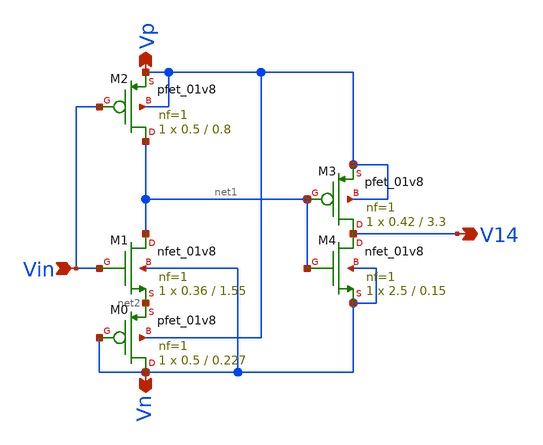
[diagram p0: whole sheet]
** sch_path: xschem/Vth_sch/Symbol/th14.sch
**.subckt th14 Vn Vp Vin V14
*.opin Vn
*.opin Vp
*.ipin Vin
*.opin V14
XM3 V14 net1 Vp Vp sky130_fd_pr__pfet_01v8 L=3.3 W=0.42 nf=1 ad='int((nf+1)/2) * W/nf * 0.29' as='int((nf+2)/2) * W/nf * 0.29'
+ pd='2*int((nf+1)/2) * (W/nf + 0.29)' ps='2*int((nf+2)/2) * (W/nf + 0.29)' nrd='0.29 / W' nrs='0.29 / W'
+ sa=0 sb=0 sd=0 mult=1 m=1
XM4 V14 net1 Vn Vn sky130_fd_pr__nfet_01v8 L=0.15 W=2.5 nf=1 ad='int((nf+1)/2) * W/nf * 0.29' as='int((nf+2)/2) * W/nf * 0.29'
+ pd='2*int((nf+1)/2) * (W/nf + 0.29)' ps='2*int((nf+2)/2) * (W/nf + 0.29)' nrd='0.29 / W' nrs='0.29 / W'
+ sa=0 sb=0 sd=0 mult=1 m=1
XM2 net1 Vin Vp Vp sky130_fd_pr__pfet_01v8 L=0.8 W=0.5 nf=1 ad='int((nf+1)/2) * W/nf * 0.29' as='int((nf+2)/2) * W/nf * 0.29'
+ pd='2*int((nf+1)/2) * (W/nf + 0.29)' ps='2*int((nf+2)/2) * (W/nf + 0.29)' nrd='0.29 / W' nrs='0.29 / W'
+ sa=0 sb=0 sd=0 mult=1 m=1
XM1 net1 Vin net2 Vn sky130_fd_pr__nfet_01v8 L=1.55 W=0.36 nf=1 ad='int((nf+1)/2) * W/nf * 0.29' as='int((nf+2)/2) * W/nf * 0.29'
+ pd='2*int((nf+1)/2) * (W/nf + 0.29)' ps='2*int((nf+2)/2) * (W/nf + 0.29)' nrd='0.29 / W' nrs='0.29 / W'
+ sa=0 sb=0 sd=0 mult=1 m=1
XM0 Vn Vn net2 Vp sky130_fd_pr__pfet_01v8 L=0.227 W=0.5 nf=1 ad='int((nf+1)/2) * W/nf * 0.29' as='int((nf+2)/2) * W/nf * 0.29'
+ pd='2*int((nf+1)/2) * (W/nf + 0.29)' ps='2*int((nf+2)/2) * (W/nf + 0.29)' nrd='0.29 / W' nrs='0.29 / W'
+ sa=0 sb=0 sd=0 mult=1 m=1
**.ends
.end
